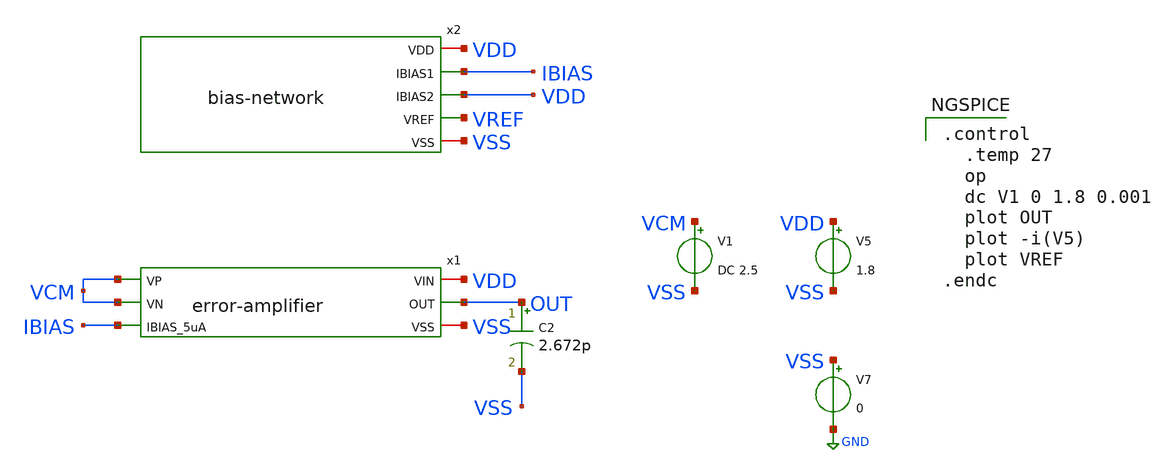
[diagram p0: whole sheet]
** sch_path: xschem/error-amplifier/testbench/tb_dc.sch
**.subckt tb_dc
C2 OUT VSS 2.672p m=1
V5 VDD VSS 1.8
V7 VSS GND 0
V1 VCM VSS DC 2.5
x1 VDD VCM VCM IBIAS OUT VSS error-amplifier
x2 VDD IBIAS VDD VREF VSS bias-network
**** begin user architecture code

.control
  .temp 27
  op
  dc V1 0 1.8 0.001
  plot OUT
  plot -i(V5)
  plot VREF
.endc




** opencircuitdesign pdks install
.lib $::SKYWATER_MODELS/sky130.lib.spice tt


**** end user architecture code
**.ends

* expanding   symbol:
*+  /foss/designs/2026/tt_sky26b_ldo_andriansyah/xschem/error-amplifier/error-amplifier.sym # of pins=6
** sym_path: xschem/error-amplifier/error-amplifier.sym
** sch_path: xschem/error-amplifier/error-amplifier.sch
.subckt error-amplifier VIN VP VN IBIAS_5uA OUT VSS
*.ipin IBIAS_5uA
*.ipin VN
*.ipin VP
*.iopin VIN
*.iopin VSS
*.opin OUT
XM1 net2 net2 VSS VSS sky130_fd_pr__nfet_01v8 L=0.6 W=4.2 nf=4 ad='int((nf+1)/2) * W/nf * 0.29' as='int((nf+2)/2) * W/nf * 0.29'
+ pd='2*int((nf+1)/2) * (W/nf + 0.29)' ps='2*int((nf+2)/2) * (W/nf + 0.29)' nrd='0.29 / W' nrs='0.29 / W'
+ sa=0 sb=0 sd=0 mult=1 m=1
XM2 OUT net2 VSS VSS sky130_fd_pr__nfet_01v8 L=0.6 W=4.2 nf=4 ad='int((nf+1)/2) * W/nf * 0.29' as='int((nf+2)/2) * W/nf * 0.29'
+ pd='2*int((nf+1)/2) * (W/nf + 0.29)' ps='2*int((nf+2)/2) * (W/nf + 0.29)' nrd='0.29 / W' nrs='0.29 / W'
+ sa=0 sb=0 sd=0 mult=1 m=1
XM3 net2 VN net1 VDD sky130_fd_pr__pfet_01v8 L=0.6 W=14 nf=4 ad='int((nf+1)/2) * W/nf * 0.29' as='int((nf+2)/2) * W/nf * 0.29'
+ pd='2*int((nf+1)/2) * (W/nf + 0.29)' ps='2*int((nf+2)/2) * (W/nf + 0.29)' nrd='0.29 / W' nrs='0.29 / W'
+ sa=0 sb=0 sd=0 mult=2 m=2
XM4 OUT VP net1 VDD sky130_fd_pr__pfet_01v8 L=0.6 W=14 nf=4 ad='int((nf+1)/2) * W/nf * 0.29' as='int((nf+2)/2) * W/nf * 0.29'
+ pd='2*int((nf+1)/2) * (W/nf + 0.29)' ps='2*int((nf+2)/2) * (W/nf + 0.29)' nrd='0.29 / W' nrs='0.29 / W'
+ sa=0 sb=0 sd=0 mult=2 m=2
XM5 net1 IBIAS_5uA VIN VIN sky130_fd_pr__pfet_01v8 L=0.6 W=6.6 nf=4 ad='int((nf+1)/2) * W/nf * 0.29'
+ as='int((nf+2)/2) * W/nf * 0.29' pd='2*int((nf+1)/2) * (W/nf + 0.29)' ps='2*int((nf+2)/2) * (W/nf + 0.29)'
+ nrd='0.29 / W' nrs='0.29 / W' sa=0 sb=0 sd=0 mult=1 m=1
XM6 IBIAS_5uA IBIAS_5uA VIN VIN sky130_fd_pr__pfet_01v8 L=0.6 W=6.6 nf=4 ad='int((nf+1)/2) * W/nf * 0.29'
+ as='int((nf+2)/2) * W/nf * 0.29' pd='2*int((nf+1)/2) * (W/nf + 0.29)' ps='2*int((nf+2)/2) * (W/nf + 0.29)'
+ nrd='0.29 / W' nrs='0.29 / W' sa=0 sb=0 sd=0 mult=1 m=1
.ends


* expanding   symbol:
*+  /foss/designs/2026/tt_sky26b_ldo_andriansyah/xschem/bias-net/schematics/bias-network.sym # of pins=5
** sym_path: xschem/bias-net/schematics/bias-network.sym
** sch_path: xschem/bias-net/schematics/bias-network.sch
.subckt bias-network VDD IBIAS1 IBIAS2 VREF VSS
*.iopin VDD
*.iopin VSS
*.opin IBIAS1
*.opin IBIAS2
*.opin VREF
XM2 VREF VREF VSS VSS sky130_fd_pr__nfet_01v8 L=2 W=3 nf=4 ad='int((nf+1)/2) * W/nf * 0.29' as='int((nf+2)/2) * W/nf * 0.29'
+ pd='2*int((nf+1)/2) * (W/nf + 0.29)' ps='2*int((nf+2)/2) * (W/nf + 0.29)' nrd='0.29 / W' nrs='0.29 / W'
+ sa=0 sb=0 sd=0 mult=2 m=2
XR1 VREF net1 VSS sky130_fd_pr__res_xhigh_po_0p69 L=6.9 mult=1 m=1
XR2 net2 net1 VSS sky130_fd_pr__res_xhigh_po_0p69 L=6.9 mult=1 m=1
XR3 net2 net3 VSS sky130_fd_pr__res_xhigh_po_0p69 L=6.9 mult=1 m=1
XR4 net4 net3 VSS sky130_fd_pr__res_xhigh_po_0p69 L=6.9 mult=1 m=1
XR5 net4 net5 VSS sky130_fd_pr__res_xhigh_po_0p69 L=6.9 mult=1 m=1
XR6 net9 net10 VSS sky130_fd_pr__res_xhigh_po_0p69 L=6.9 mult=1 m=1
XR7 net9 net8 VSS sky130_fd_pr__res_xhigh_po_0p69 L=6.9 mult=1 m=1
XR8 net7 net8 VSS sky130_fd_pr__res_xhigh_po_0p69 L=6.9 mult=1 m=1
XR9 net7 net6 VSS sky130_fd_pr__res_xhigh_po_0p69 L=6.9 mult=1 m=1
XR10 net5 net6 VSS sky130_fd_pr__res_xhigh_po_0p69 L=6.9 mult=1 m=1
XM1 IBIAS1 VREF VSS VSS sky130_fd_pr__nfet_01v8 L=2 W=3 nf=4 ad='int((nf+1)/2) * W/nf * 0.29' as='int((nf+2)/2) * W/nf * 0.29'
+ pd='2*int((nf+1)/2) * (W/nf + 0.29)' ps='2*int((nf+2)/2) * (W/nf + 0.29)' nrd='0.29 / W' nrs='0.29 / W'
+ sa=0 sb=0 sd=0 mult=2 m=2
XM3 IBIAS2 VREF VSS VSS sky130_fd_pr__nfet_01v8 L=2 W=3 nf=4 ad='int((nf+1)/2) * W/nf * 0.29' as='int((nf+2)/2) * W/nf * 0.29'
+ pd='2*int((nf+1)/2) * (W/nf + 0.29)' ps='2*int((nf+2)/2) * (W/nf + 0.29)' nrd='0.29 / W' nrs='0.29 / W'
+ sa=0 sb=0 sd=0 mult=2 m=2
XR11 net10 net11 VSS sky130_fd_pr__res_xhigh_po_0p69 L=6.9 mult=1 m=1
XR12 net12 net11 VSS sky130_fd_pr__res_xhigh_po_0p69 L=6.9 mult=1 m=1
XR13 net12 net13 VSS sky130_fd_pr__res_xhigh_po_0p69 L=6.9 mult=1 m=1
XR14 net14 net13 VSS sky130_fd_pr__res_xhigh_po_0p69 L=6.9 mult=1 m=1
XR15 net14 net15 VSS sky130_fd_pr__res_xhigh_po_0p69 L=6.9 mult=1 m=1
XR16 net19 VDD VSS sky130_fd_pr__res_xhigh_po_0p69 L=6.9 mult=1 m=1
XR17 net19 net18 VSS sky130_fd_pr__res_xhigh_po_0p69 L=6.9 mult=1 m=1
XR18 net17 net18 VSS sky130_fd_pr__res_xhigh_po_0p69 L=6.9 mult=1 m=1
XR19 net17 net16 VSS sky130_fd_pr__res_xhigh_po_0p69 L=6.9 mult=1 m=1
XR20 net15 net16 VSS sky130_fd_pr__res_xhigh_po_0p69 L=6.9 mult=1 m=1
XR21 VSS VSS VSS sky130_fd_pr__res_xhigh_po_0p69 L=6.9 mult=1 m=1
XR22 VSS VSS VSS sky130_fd_pr__res_xhigh_po_0p69 L=6.9 mult=1 m=1
.ends

.GLOBAL GND
.end
